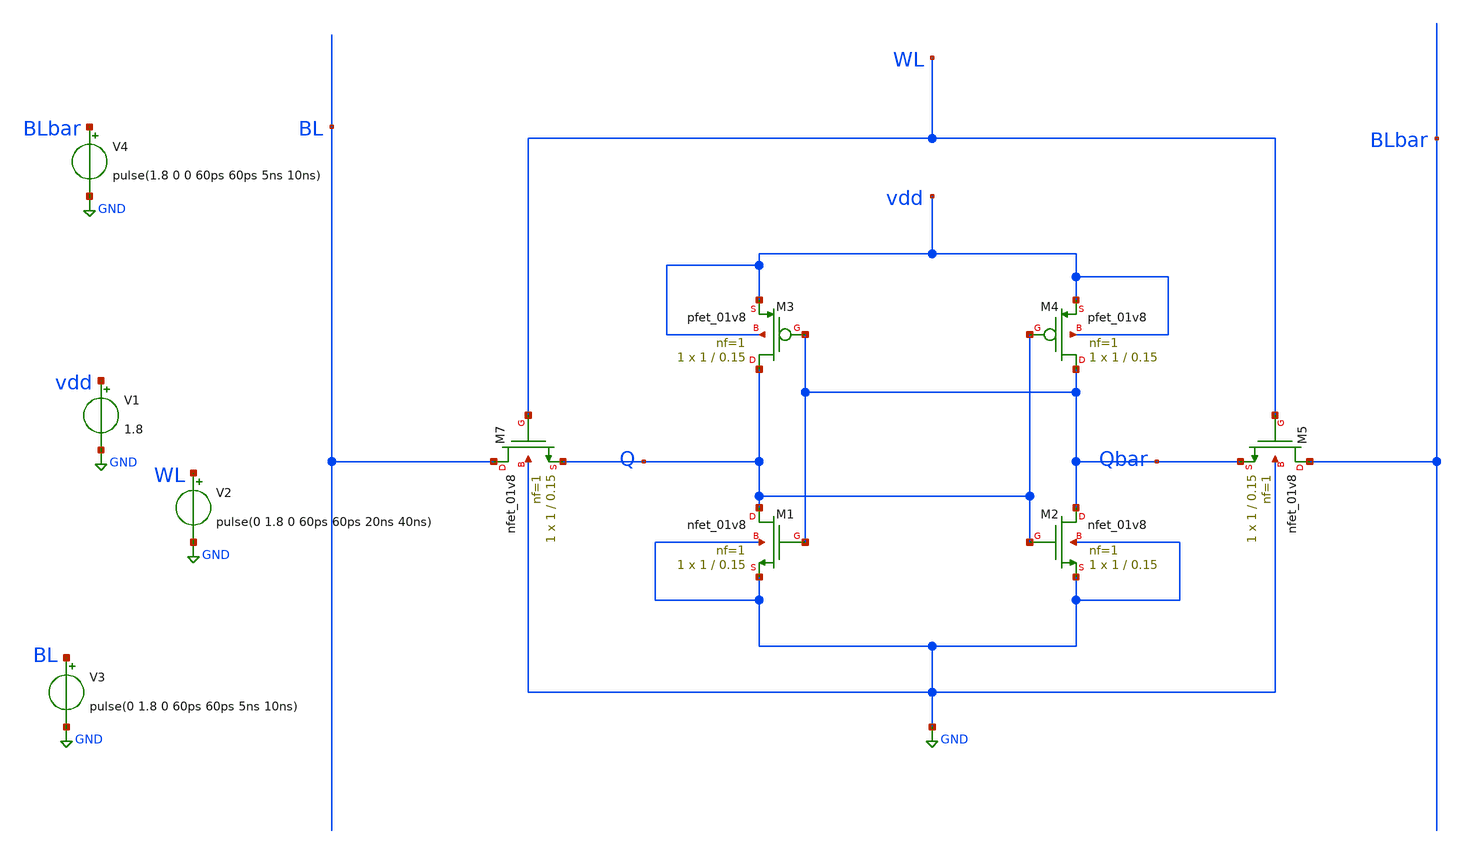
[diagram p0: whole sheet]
** sch_path: sram_6T_write.sch
**.subckt sram_6T_write
XM1 Q Qbar GND GND sky130_fd_pr__nfet_01v8 L=0.15 W=1 nf=1 ad='int((nf+1)/2) * W/nf * 0.29' as='int((nf+2)/2) * W/nf * 0.29'
+ pd='2*int((nf+1)/2) * (W/nf + 0.29)' ps='2*int((nf+2)/2) * (W/nf + 0.29)' nrd='0.29 / W' nrs='0.29 / W'
+ sa=0 sb=0 sd=0 mult=1 m=1
XM2 Qbar Q GND GND sky130_fd_pr__nfet_01v8 L=0.15 W=1 nf=1 ad='int((nf+1)/2) * W/nf * 0.29' as='int((nf+2)/2) * W/nf * 0.29'
+ pd='2*int((nf+1)/2) * (W/nf + 0.29)' ps='2*int((nf+2)/2) * (W/nf + 0.29)' nrd='0.29 / W' nrs='0.29 / W'
+ sa=0 sb=0 sd=0 mult=1 m=1
XM3 Q Qbar vdd vdd sky130_fd_pr__pfet_01v8 L=0.15 W=1 nf=1 ad='int((nf+1)/2) * W/nf * 0.29' as='int((nf+2)/2) * W/nf * 0.29'
+ pd='2*int((nf+1)/2) * (W/nf + 0.29)' ps='2*int((nf+2)/2) * (W/nf + 0.29)' nrd='0.29 / W' nrs='0.29 / W'
+ sa=0 sb=0 sd=0 mult=1 m=1
XM4 Qbar Q vdd vdd sky130_fd_pr__pfet_01v8 L=0.15 W=1 nf=1 ad='int((nf+1)/2) * W/nf * 0.29' as='int((nf+2)/2) * W/nf * 0.29'
+ pd='2*int((nf+1)/2) * (W/nf + 0.29)' ps='2*int((nf+2)/2) * (W/nf + 0.29)' nrd='0.29 / W' nrs='0.29 / W'
+ sa=0 sb=0 sd=0 mult=1 m=1
XM7 BL WL Q GND sky130_fd_pr__nfet_01v8 L=0.15 W=1 nf=1 ad='int((nf+1)/2) * W/nf * 0.29' as='int((nf+2)/2) * W/nf * 0.29'
+ pd='2*int((nf+1)/2) * (W/nf + 0.29)' ps='2*int((nf+2)/2) * (W/nf + 0.29)' nrd='0.29 / W' nrs='0.29 / W'
+ sa=0 sb=0 sd=0 mult=1 m=1
XM5 BLbar WL Qbar GND sky130_fd_pr__nfet_01v8 L=0.15 W=1 nf=1 ad='int((nf+1)/2) * W/nf * 0.29' as='int((nf+2)/2) * W/nf * 0.29'
+ pd='2*int((nf+1)/2) * (W/nf + 0.29)' ps='2*int((nf+2)/2) * (W/nf + 0.29)' nrd='0.29 / W' nrs='0.29 / W'
+ sa=0 sb=0 sd=0 mult=1 m=1
V1 vdd GND 1.8
V2 WL GND pulse(0 1.8 0 60ps 60ps 20ns 40ns)
V3 BL GND pulse(0 1.8 0 60ps 60ps 5ns 10ns)
V4 BLbar GND pulse(1.8 0 0 60ps 60ps 5ns 10ns)
**** begin user architecture code


.lib /home/asashirokenpachi/.volare/sky130B/libs.tech/ngspice/sky130.lib.spice tt
.tran 0.1n 100n
.control
run
plot V(wl)+8 V(bl)+2 V(blbar) V(q)+6 V(qbar)+4
.endc
.end

**** end user architecture code
**.ends
.GLOBAL GND
.end
